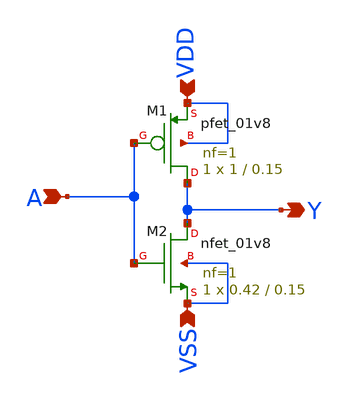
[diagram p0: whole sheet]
** sch_path: buffer/design_circuit/invx1.sch
**.subckt invx1 A Y VDD VSS
*.ipin A
*.opin Y
*.ipin VDD
*.ipin VSS
XM1 Y A VDD VDD sky130_fd_pr__pfet_01v8 L=0.15 W=1 nf=1 ad='int((nf+1)/2) * W/nf * 0.29' as='int((nf+2)/2) * W/nf * 0.29'
+ pd='2*int((nf+1)/2) * (W/nf + 0.29)' ps='2*int((nf+2)/2) * (W/nf + 0.29)' nrd='0.29 / W' nrs='0.29 / W'
+ sa=0 sb=0 sd=0 mult=1 m=1
XM2 Y A VSS VSS sky130_fd_pr__nfet_01v8 L=0.15 W=0.42 nf=1 ad='int((nf+1)/2) * W/nf * 0.29' as='int((nf+2)/2) * W/nf * 0.29'
+ pd='2*int((nf+1)/2) * (W/nf + 0.29)' ps='2*int((nf+2)/2) * (W/nf + 0.29)' nrd='0.29 / W' nrs='0.29 / W'
+ sa=0 sb=0 sd=0 mult=1 m=1
**.ends
.end
